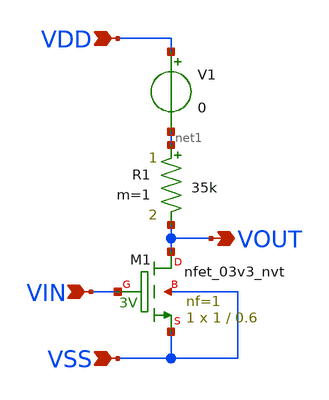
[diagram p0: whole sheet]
** sch_path: design/THESIS_EXP_RO_INVERTER_SKY130A/INV_NVT_R.sch
**.subckt INV_NVT_R VDD VSS VIN VOUT
*.ipin VDD
*.ipin VSS
*.ipin VIN
*.opin VOUT
R1 net1 VOUT 35k m=1
XM1 VOUT VIN VSS VSS sky130_fd_pr__nfet_03v3_nvt L=0.6 W=1 nf=1 ad='int((nf+1)/2) * W/nf * 0.29' as='int((nf+2)/2) * W/nf * 0.29'
+ pd='2*int((nf+1)/2) * (W/nf + 0.29)' ps='2*int((nf+2)/2) * (W/nf + 0.29)' nrd='0.29 / W' nrs='0.29 / W'
+ sa=0 sb=0 sd=0 mult=1 m=1
V1 VDD net1 0
.save i(v1)
**.ends
.end
